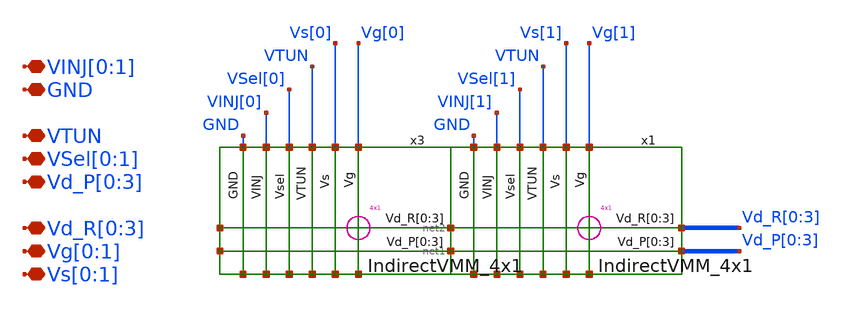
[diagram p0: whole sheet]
** sch_path: ihp130_cells/IndirectVMM_4x2/IndirectVMM_4x2.sch
**.subckt IndirectVMM_4x2 Vd_R[0],Vd_R[1],Vd_R[2],Vd_R[3] Vd_P[0],Vd_P[1],Vd_P[2],Vd_P[3]
*+ Vg[0],Vg[1] VTUN VSel[0],VSel[1] GND VINJ[0],VINJ[1] Vs[0],Vs[1]
*.iopin Vd_R[0],Vd_R[1],Vd_R[2],Vd_R[3]
*.iopin Vd_P[0],Vd_P[1],Vd_P[2],Vd_P[3]
*.iopin Vg[0],Vg[1]
*.iopin VTUN
*.iopin VSel[0],VSel[1]
*.iopin GND
*.iopin VINJ[0],VINJ[1]
*.iopin Vs[0],Vs[1]
x3 net1[3] net1[2] net1[1] net1[0] net2[3] net2[2] net2[1] net2[0] Vg[0] Vs[0] VTUN VSel[0] VINJ[0]
+ GND net3[3] net3[2] net3[1] net3[0] net4[3] net4[2] net4[1] net4[0] net5 IndirectVMM_4x1
x1 Vd_P[0] Vd_P[1] Vd_P[2] Vd_P[3] Vd_R[0] Vd_R[1] Vd_R[2] Vd_R[3] Vg[1] Vs[1] VTUN VSel[1] VINJ[1]
+ GND net2[3] net2[2] net2[1] net2[0] net1[3] net1[2] net1[1] net1[0] net6 IndirectVMM_4x1
**.ends
.end
